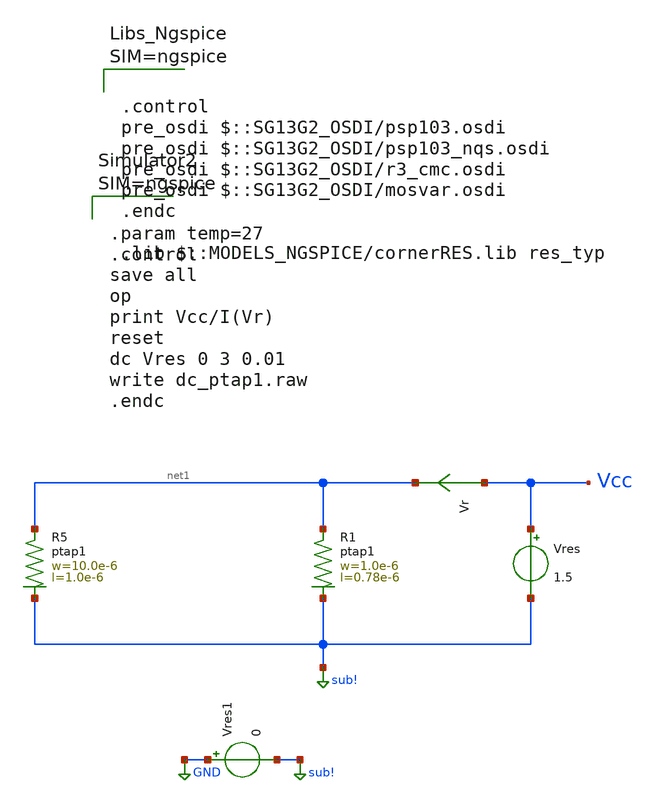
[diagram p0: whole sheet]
** sch_path: ihp-sg13g2/xschem_libs/sg13g2_tests/dc_ptap1/schematic/dc_ptap1.sch
* Copyright 2023 IHP PDK Authors
**.subckt dc_ptap1
Vres Vcc sub! 1.5
Vr Vcc net1 0
.save i(vr)
XR5 net1 sub! ptap1 R=30.62 w=10.0e-6 l=1.0e-6
XR1 net1 sub! ptap1 R=225.8 w=1.0e-6 l=0.78e-6
Vres1 GND sub! 0
**** begin user architecture code

.control
pre_osdi $::SG13G2_OSDI/psp103.osdi
pre_osdi $::SG13G2_OSDI/psp103_nqs.osdi
pre_osdi $::SG13G2_OSDI/r3_cmc.osdi
pre_osdi $::SG13G2_OSDI/mosvar.osdi
.endc

.lib $::MODELS_NGSPICE/cornerRES.lib res_typ




.param temp=27
.control
save all
op
print Vcc/I(Vr)
reset
dc Vres 0 3 0.01
write dc_ptap1.raw
.endc



**** end user architecture code
**.ends
.GLOBAL GND
.GLOBAL sub!
.end
